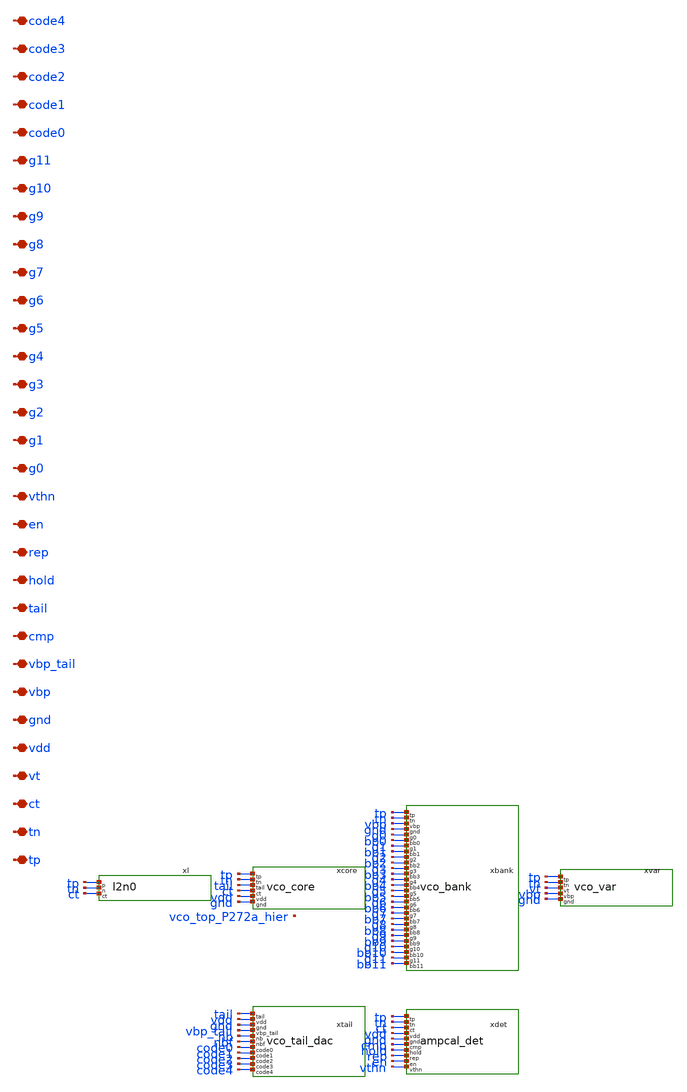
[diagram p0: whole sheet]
** sch_path: analog/vco/sch/vco_top.sch
**.subckt vco_top tp tn ct vt vdd gnd vbp vbp_tail cmp tail hold rep en vthn g0 g1 g2 g3 g4 g5 g6 g7
*+ g8 g9 g10 g11 code0 code1 code2 code3 code4
*.iopin tp
*.iopin tn
*.iopin ct
*.iopin vt
*.iopin vdd
*.iopin gnd
*.iopin vbp
*.iopin vbp_tail
*.iopin cmp
*.iopin tail
*.iopin hold
*.iopin rep
*.iopin en
*.iopin vthn
*.iopin g0
*.iopin g1
*.iopin g2
*.iopin g3
*.iopin g4
*.iopin g5
*.iopin g6
*.iopin g7
*.iopin g8
*.iopin g9
*.iopin g10
*.iopin g11
*.iopin code0
*.iopin code1
*.iopin code2
*.iopin code3
*.iopin code4
xl tp tn ct l2n0
xcore tp tn tail ct vdd gnd vco_core
xbank tp tn vbp gnd g0 bb0 g1 bb1 g2 bb2 g3 bb3 g4 bb4 g5 bb5 g6 bb6 g7 bb7 g8 bb8 g9 bb9 g10 bb10
+ g11 bb11 vco_bank
xvar tp tn vt vbp gnd vco_var
xtail tail vdd gnd vbp_tail nb nbf code0 code1 code2 code3 code4 vco_tail_dac
xdet tp tn ct vdd gnd cmp hold rep en vthn ampcal_det
**.ends
.end
